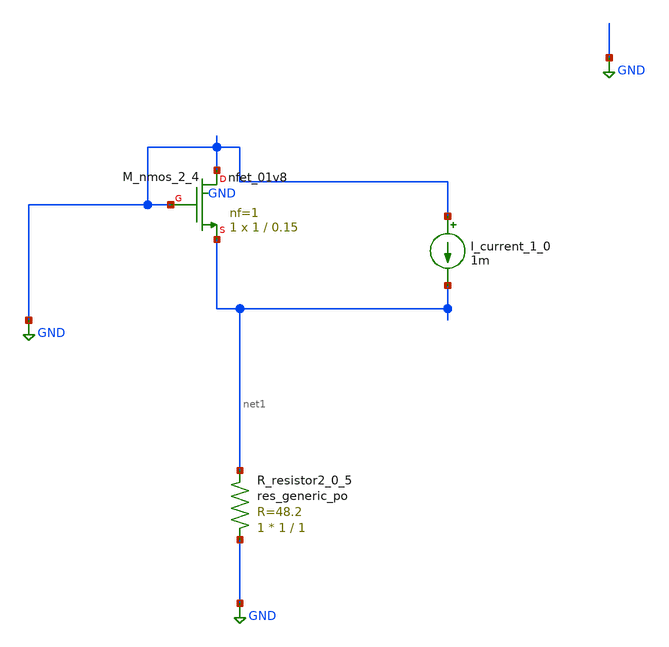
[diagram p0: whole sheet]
** sch_path: schematics/AMSNet/452.sch
**.subckt 452
I_current_1_0 GND net1 1m
XM_nmos_2_4 GND GND net1 GND sky130_fd_pr__nfet_01v8 L=0.15 W=1 nf=1 ad='int((1 + 1)/2) * 1 / 1 * 0.29'
+ as='int((1 + 2)/2) * 1 / 1 * 0.29' pd='2*int((1 + 1)/2) * (1 / 1 + 0.29)' ps='2*int((1 + 2)/2) * (1 / 1 + 0.29)'
+ nrd='0.29 / 1 ' nrs='0.29 / 1 ' sa=0 sb=0 sd=0 mult=1 m=1
XR_resistor2_0_5 GND net1 sky130_fd_pr__res_generic_po W=1 L=1 m=1
**.ends
.GLOBAL GND
.end
